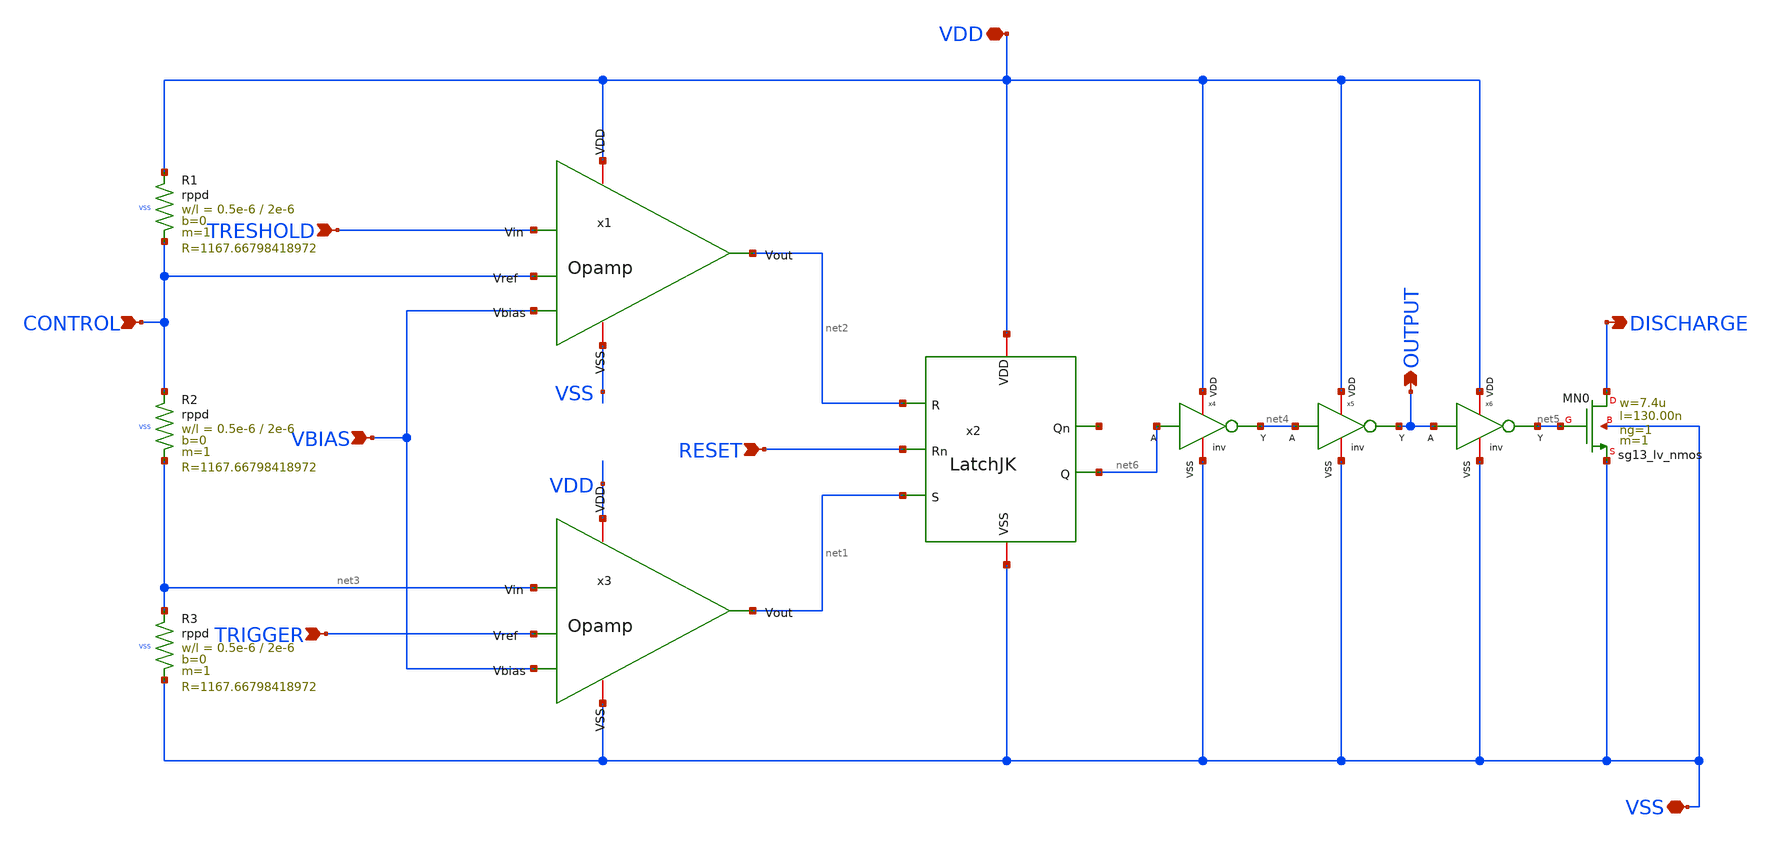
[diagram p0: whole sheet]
** sch_path: schematic/555.sch
**.subckt 555 OUTPUT TRIGGER VSS RESET TRESHOLD DISCHARGE VBIAS CONTROL VDD
*.opin OUTPUT
*.ipin TRIGGER
*.iopin VSS
*.ipin RESET
*.ipin TRESHOLD
*.opin DISCHARGE
*.ipin VBIAS
*.ipin CONTROL
*.iopin VDD
x1 VDD TRESHOLD CONTROL net2 VBIAS VSS Opamp
x2 VDD net1 net7 net6 net2 RESET VSS LatchJK
x3 VDD net3 TRIGGER net1 VBIAS VSS Opamp
XMN0 DISCHARGE net5 VSS VSS sg13_lv_nmos w=7.4u l=130.00n ng=1 m=1 mm_ok=1
x4 VDD net4 net6 VSS inv
x5 VDD OUTPUT net4 VSS inv
x6 VDD net5 OUTPUT VSS inv
XR1 VDD CONTROL VSS rppd w=0.5e-6 l=2e-6 m=1 b=0 mm_ok=1
XR2 CONTROL net3 VSS rppd w=0.5e-6 l=2e-6 m=1 b=0 mm_ok=1
XR3 net3 VSS VSS rppd w=0.5e-6 l=2e-6 m=1 b=0 mm_ok=1
**.ends
.end
